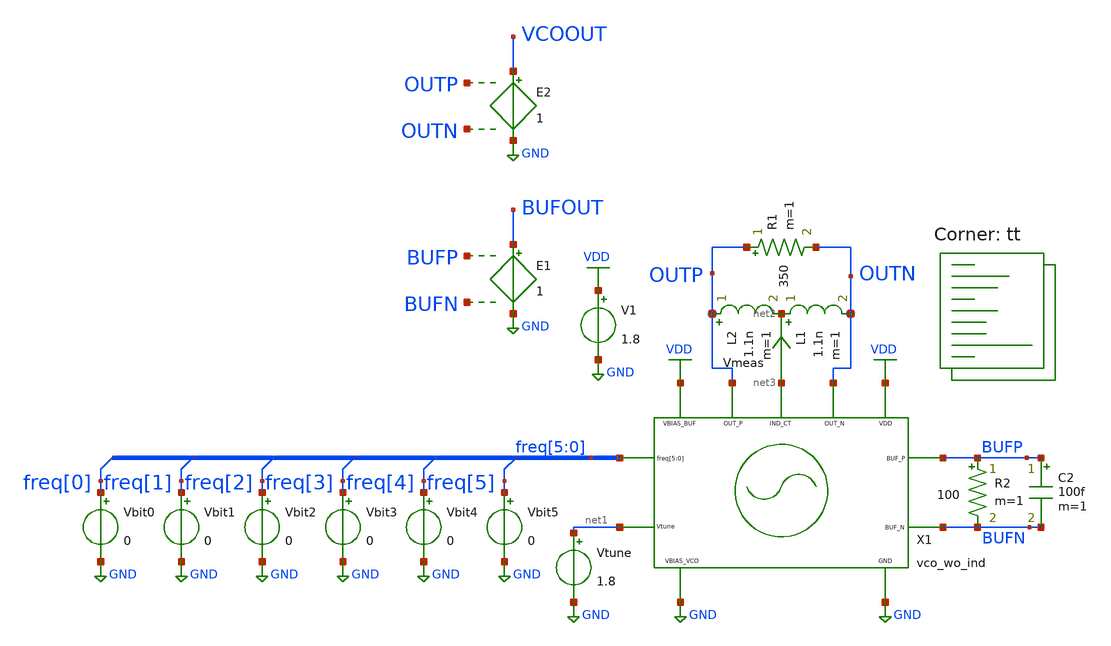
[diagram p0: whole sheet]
** sch_path: xschem/vco/testbenches/top/vco_wo_ind_sweep.sch
**.subckt vco_wo_ind_sweep
V1 VDD GND 1.8
Vbit0 freq[0] GND 0
Vbit1 freq[1] GND 0
Vbit2 freq[2] GND 0
Vbit3 freq[3] GND 0
Vbit4 freq[4] GND 0
Vbit5 freq[5] GND 0
L1 net2 OUTN 1.1n m=1
L2 OUTP net2 1.1n m=1
Vtune net1 GND 1.8
R1 OUTP OUTN 350 m=1
R2 BUFP BUFN 100 m=1
C2 BUFP BUFN 100f m=1
E1 BUFOUT GND BUFP BUFN 1
E2 VCOOUT GND OUTP OUTN 1
X1 OUTP GND net3 VDD OUTN freq[5] freq[4] freq[3] freq[2] freq[1] freq[0] GND net1 BUFP BUFN VDD
+ vco_wo_ind
Vmeas net3 net2 0
.save i(vmeas)
**** begin user architecture code


.ic v(outp) = 0.8265 v(outn)= 0.8267
.save vcoout bufout outp outn Vbit0 Vbit1 Vbit2 Vbit3 Vbit4 Vbit5
.control
    *intial value of code sweeps
    let code = 0
    let code_end = 64
    let code_bits = vector(6)
    let bit_count = 0
    let i = 0
    let vtune_step = 0.1
    let len = 19

    *creating plot to store amplitude and freq data
    setplot new
    set scratch = $curplot
    set curplottitle = "Frequency and Amplitude for each code"
    let vtune_scale = vtune_step*vector(len)
    settype voltage vtune_scale
    let freq = unitvec(code_end*len)
    reshape freq [64][19]
    settype frequency freq
    let amplitude = unitvec(code_end*len)
    reshape amplitude [64][19]
    settype voltage amplitude

    *setting printing data
    set wr_singlescale
    set wr_vecnames

    echo "==========================="
    echo "SIMULATION STARTED AT TIME:"
    shell date +%H:%M
    echo "==========================="
    while code < code_end
    * setting the cap bank code
        let tmp = code
        while bit_count < 6
            let tmp = bit_count ? floor(tmp/2) : tmp
            let code_bits[bit_count] = tmp ? tmp % 2 : 0
            let bit_count = bit_count +  1
        end
        let bit_count = 0
        print code_bits
        alter vbit0 1.8*code_bits[0]
        alter vbit1 1.8*code_bits[1]
        alter vbit2 1.8*code_bits[2]
        alter vbit3 1.8*code_bits[3]
        alter vbit4 1.8*code_bits[4]
        alter vbit5 1.8*code_bits[5]

        *sweeping vtune voltage
        while i < len
            alter vtune i*vtune_step
            tran 10p 1n
            meas tran period trig vcoout val=0.2 rise=2 targ vcoout val=0.2 rise=3
            let {$scratch}.freq[code][i] = 1/period
            let {$scratch}.amplitude[code][i] = maximum(bufout)
            let i = i + 1
        end
        *reset variables
        let i = 0
        let code = code + 1
    end

    *plotting
    setplot {$scratch}
    wrdata data.txt freq amplitude
    plot freq
    echo "==========================="
    echo "SIMULATION ENDED AT TIME:"
    shell date +%H:%M
    echo "==========================="
.endc


.lib $::SKYWATER_MODELS/sky130.lib.spice tt
**** end user architecture code
**.ends
.GLOBAL GND
.GLOBAL VDD
.end
